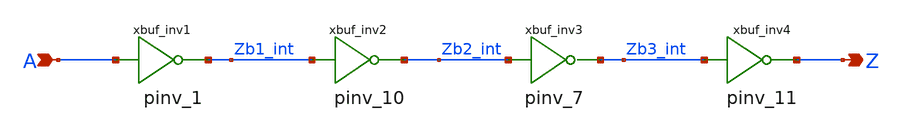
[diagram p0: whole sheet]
** sch_path: sram_2_64_scn4m/pdriver_2.sch
**.subckt pdriver_2 A Z
*.ipin A
*.opin Z
xbuf_inv1 A Zb1_int vdd gnd pinv_1
xbuf_inv2 Zb1_int Zb2_int vdd gnd pinv_10
xbuf_inv3 Zb2_int Zb3_int vdd gnd pinv_7
xbuf_inv4 Zb3_int Z gnd gnd pinv_11
**.ends

* expanding   symbol:  pinv_1.sym # of pins=2
** sym_path: sram_2_64_scn4m_lcc/pinv_1.sym
** sch_path: sram_2_64_scn4m_lcc/pinv_1.sch
.subckt pinv_1 A Z vdd gnd
*.ipin A
*.opin Z
Mpinv_nmos Z A gnd gnd n w=0.8u l=0.4u m=1
Mp_inv_pmos Z A vdd vdd p w=6.4u l=0.4u m=1
.ends


* expanding   symbol:  pinv_10.sym # of pins=2
** sym_path: sram_2_64_scn4m/pinv_10.sym
** sch_path: sram_2_64_scn4m/pinv_10.sch
.subckt pinv_10 A Z vdd gnd
*.ipin A
*.opin Z
*.iopin vdd
*.iopin gnd
XMpinv_nmos Z A gnd gnd sky130_fd_pr__nfet_01v8 L=0.4 W=0.8 nf=1 ad='int((nf+1)/2) * W/nf * 0.29' as='int((nf+2)/2) * W/nf * 0.29'
+ pd='2*int((nf+1)/2) * (W/nf + 0.29)' ps='2*int((nf+2)/2) * (W/nf + 0.29)' nrd='0.29 / W' nrs='0.29 / W'
+ sa=0 sb=0 sd=0 mult=1 m=1
XMpinv_pmos Z A vdd vdd sky130_fd_pr__pfet_01v8 L=0.4 W=1.6 nf=1 ad='int((nf+1)/2) * W/nf * 0.29' as='int((nf+2)/2) * W/nf * 0.29'
+ pd='2*int((nf+1)/2) * (W/nf + 0.29)' ps='2*int((nf+2)/2) * (W/nf + 0.29)' nrd='0.29 / W' nrs='0.29 / W'
+ sa=0 sb=0 sd=0 mult=1 m=1
.ends


* expanding   symbol:  pinv_7.sym # of pins=2
** sym_path: sram_2_16_scn4m/pinv_7.sym
** sch_path: sram_2_16_scn4m/pinv_7.sch
.subckt pinv_7 A Z vdd gnd
*.ipin A
*.opin Z
Mpinv_nmos Z A gnd gnd n w=4.0u l=0.4u m=3
Mp_inv_pmos Z A vdd vdd p w=8.0u l=0.4u m=3
.ends


* expanding   symbol:  pinv_11.sym # of pins=2
** sym_path: sram_2_64_scn4m/pinv_11.sym
** sch_path: sram_2_64_scn4m/pinv_11.sch
.subckt pinv_11 A Z vdd gnd
*.ipin A
*.opin Z
*.iopin vdd
*.iopin gnd
XM2 Z A gnd gnd sky130_fd_pr__nfet_01v8 L=0.4 W=4.0 nf=1 ad='int((nf+1)/2) * W/nf * 0.29' as='int((nf+2)/2) * W/nf * 0.29'
+ pd='2*int((nf+1)/2) * (W/nf + 0.29)' ps='2*int((nf+2)/2) * (W/nf + 0.29)' nrd='0.29 / W' nrs='0.29 / W'
+ sa=0 sb=0 sd=0 mult=1 m=1
XM3 Z A vdd vdd sky130_fd_pr__pfet_01v8 L=0.4 W=8.0 nf=1 ad='int((nf+1)/2) * W/nf * 0.29' as='int((nf+2)/2) * W/nf * 0.29'
+ pd='2*int((nf+1)/2) * (W/nf + 0.29)' ps='2*int((nf+2)/2) * (W/nf + 0.29)' nrd='0.29 / W' nrs='0.29 / W'
+ sa=0 sb=0 sd=0 mult=1 m=1
.ends

.end
